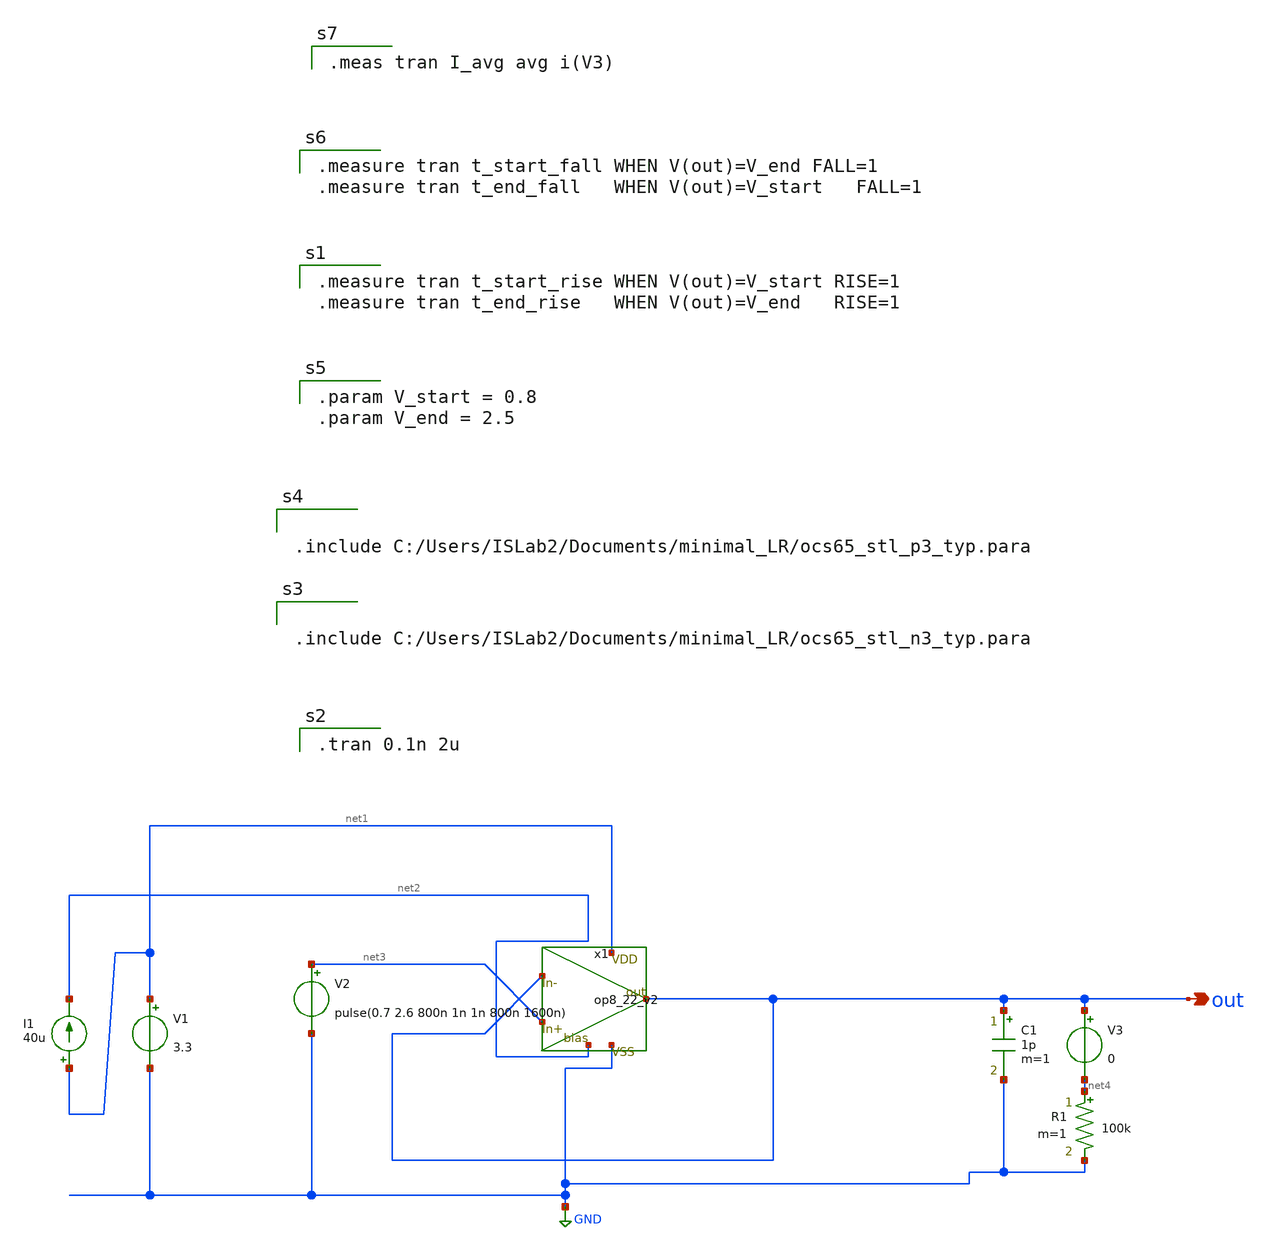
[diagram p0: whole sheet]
** sch_path: OPAmp_sim_SR.sch
**.subckt OPAmp_sim_SR out
*.opin out
V1 net1 GND 3.3
V2 net3 GND pulse(0.7 2.6 800n 1n 1n 800n 1600n)
I1 net1 net2 40u
V3 out net4 0
R1 net4 GND 100k m=1
C1 out GND 1p m=1
x1 net3 out net1 GND net2 out op8_22_v2
**** begin user architecture code

.tran 0.1n 2u


.param V_start = 0.8
.param V_end = 2.5


.measure tran t_start_rise WHEN V(out)=V_start RISE=1
.measure tran t_end_rise   WHEN V(out)=V_end   RISE=1


.measure tran t_start_fall WHEN V(out)=V_end FALL=1
.measure tran t_end_fall   WHEN V(out)=V_start   FALL=1



.include C:/Users/ISLab2/Documents/minimal_LR/ocs65_stl_n3_typ.para



.include C:/Users/ISLab2/Documents/minimal_LR/ocs65_stl_p3_typ.para


.meas tran I_avg avg i(V3)

**** end user architecture code
**.ends

* expanding   symbol:  C:/Users/ISLab2/Documents/minimal_LR/Xschem/op8_22_v2.sym # of pins=6
** sym_path: Xschem/op8_22_v2.sym
** sch_path: Xschem/op8_22_v2.sch
.subckt op8_22_v2 In+ In- VDD VSS bias out
*.iopin In+
*.iopin In-
*.iopin out
*.iopin VDD
*.iopin VSS
*.iopin bias
C1 net20 out 1.5p m=1
C2 out net21 1.5p m=1
M1 net5 net1 VDD VDD pch w=15u l=5u as=0 ps=0 ad=0 pd=0 m=1
M2 net6 net1 VDD VDD pch w=15u l=5u as=0 ps=0 ad=0 pd=0 m=1
M3 net7 net2 VDD VDD pch w=20u l=5u as=0 ps=0 ad=0 pd=0 m=5
M4 net4 net2 VDD VDD pch w=20u l=5u as=0 ps=0 ad=0 pd=0 m=5
M5 net3 net3 VDD VDD pch w=15u l=0.5u as=0 ps=0 ad=0 pd=0 m=10
M6 net12 net1 VDD VDD pch w=4u l=5u as=0 ps=0 ad=0 pd=0 m=1
M7 out net9 VDD VDD pch w=15u l=0.5u as=0 ps=0 ad=0 pd=0 m=30
M8 net8 net8 net3 VDD pch w=15u l=0.5u as=0 ps=0 ad=0 pd=0 m=10
M9 net2 net2 net7 VDD pch w=20u l=2u as=0 ps=0 ad=0 pd=0 m=5
M10 net9 net2 net4 VDD pch w=20u l=2u as=0 ps=0 ad=0 pd=0 m=5
M11 net1 net1 net5 VDD pch w=20u l=2u as=0 ps=0 ad=0 pd=0 m=1
M12 net10 net1 net6 VDD pch w=40u l=2u as=0 ps=0 ad=0 pd=0 m=1
M13 net15 In+ net10 net10 pch w=20u l=3u as=0 ps=0 ad=0 pd=0 m=10
M14 net14 In- net10 net10 pch w=20u l=3u as=0 ps=0 ad=0 pd=0 m=10
M15 net13 net8 net9 VDD pch w=15u l=0.5u as=0 ps=0 ad=0 pd=0 m=10
M16 net1 bias net18 VSS nch w=10u l=2u as=0 ps=0 ad=0 pd=0 m=1
M17 net18 bias VSS VSS nch w=5u l=5u as=0 ps=0 ad=0 pd=0 m=1
M18 net19 bias VSS VSS nch w=10u l=5u as=0 ps=0 ad=0 pd=0 m=1
M19 net11 bias net19 VSS nch w=20u l=2u as=0 ps=0 ad=0 pd=0 m=1
M21 net13 bias net15 VSS nch w=20u l=2u as=0 ps=0 ad=0 pd=0 m=10
M22 net8 bias VSS VSS nch w=1.5u l=5u as=0 ps=0 ad=0 pd=0 m=1
M23 out net13 VSS VSS nch w=10u l=0.5u as=0 ps=0 ad=0 pd=0 m=30
M24 bias bias net17 VSS nch w=10u l=2u as=0 ps=0 ad=0 pd=0 m=1
M25 net17 bias VSS VSS nch w=5u l=5u as=0 ps=0 ad=0 pd=0 m=1
M26 net7 In- net11 VSS nch w=20u l=3u as=0 ps=0 ad=0 pd=0 m=5
M27 net4 In+ net11 VSS nch w=20u l=3u as=0 ps=0 ad=0 pd=0 m=5
M28 net2 bias net14 VSS nch w=20u l=2u as=0 ps=0 ad=0 pd=0 m=10
M30 net9 net12 net13 VSS nch w=10u l=0.5u as=0 ps=0 ad=0 pd=0 m=5
M31 net12 net12 net16 VSS nch w=10u l=0.5u as=0 ps=0 ad=0 pd=0 m=5
M32 net16 net16 VSS VSS nch w=10u l=0.5u as=0 ps=0 ad=0 pd=0 m=5
M20 net15 bias VSS VSS nch w=10u l=5u as=0 ps=0 ad=0 pd=0 m=2
M29 net14 bias VSS VSS nch w=10u l=5u as=0 ps=0 ad=0 pd=0 m=2
R1 net9 net20 3k m=1
R2 net21 net13 3k m=1
.ends

.GLOBAL GND
.end
